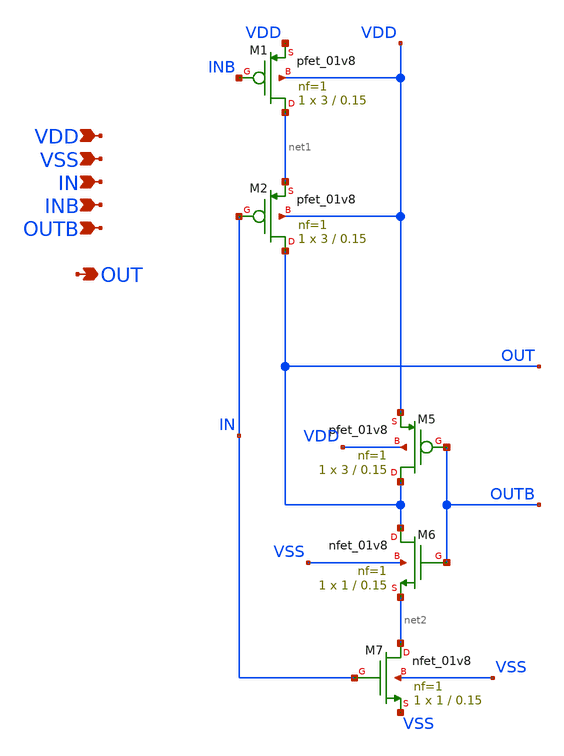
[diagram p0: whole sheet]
** sch_path: xschem/pd_in_half.sch
**.subckt pd_in_half VDD IN INB VSS OUT OUTB
*.ipin VDD
*.ipin IN
*.ipin INB
*.ipin VSS
*.opin OUT
*.ipin OUTB
XM7 net2 IN VSS VSS sky130_fd_pr__nfet_01v8 L=0.15 W=1 nf=1 ad='int((nf+1)/2) * W/nf * 0.29' as='int((nf+2)/2) * W/nf * 0.29'
+ pd='2*int((nf+1)/2) * (W/nf + 0.29)' ps='2*int((nf+2)/2) * (W/nf + 0.29)' nrd='0.29 / W' nrs='0.29 / W'
+ sa=0 sb=0 sd=0 mult=1 m=1
XM6 OUT OUTB net2 VSS sky130_fd_pr__nfet_01v8 L=0.15 W=1 nf=1 ad='int((nf+1)/2) * W/nf * 0.29' as='int((nf+2)/2) * W/nf * 0.29'
+ pd='2*int((nf+1)/2) * (W/nf + 0.29)' ps='2*int((nf+2)/2) * (W/nf + 0.29)' nrd='0.29 / W' nrs='0.29 / W'
+ sa=0 sb=0 sd=0 mult=1 m=1
XM1 net1 INB VDD VDD sky130_fd_pr__pfet_01v8 L=0.15 W=3 nf=1 ad='int((nf+1)/2) * W/nf * 0.29' as='int((nf+2)/2) * W/nf * 0.29'
+ pd='2*int((nf+1)/2) * (W/nf + 0.29)' ps='2*int((nf+2)/2) * (W/nf + 0.29)' nrd='0.29 / W' nrs='0.29 / W'
+ sa=0 sb=0 sd=0 mult=1 m=1
XM2 OUT IN net1 VDD sky130_fd_pr__pfet_01v8 L=0.15 W=3 nf=1 ad='int((nf+1)/2) * W/nf * 0.29' as='int((nf+2)/2) * W/nf * 0.29'
+ pd='2*int((nf+1)/2) * (W/nf + 0.29)' ps='2*int((nf+2)/2) * (W/nf + 0.29)' nrd='0.29 / W' nrs='0.29 / W'
+ sa=0 sb=0 sd=0 mult=1 m=1
XM5 OUT OUTB VDD VDD sky130_fd_pr__pfet_01v8 L=0.15 W=3 nf=1 ad='int((nf+1)/2) * W/nf * 0.29' as='int((nf+2)/2) * W/nf * 0.29'
+ pd='2*int((nf+1)/2) * (W/nf + 0.29)' ps='2*int((nf+2)/2) * (W/nf + 0.29)' nrd='0.29 / W' nrs='0.29 / W'
+ sa=0 sb=0 sd=0 mult=1 m=1
**.ends
.end
